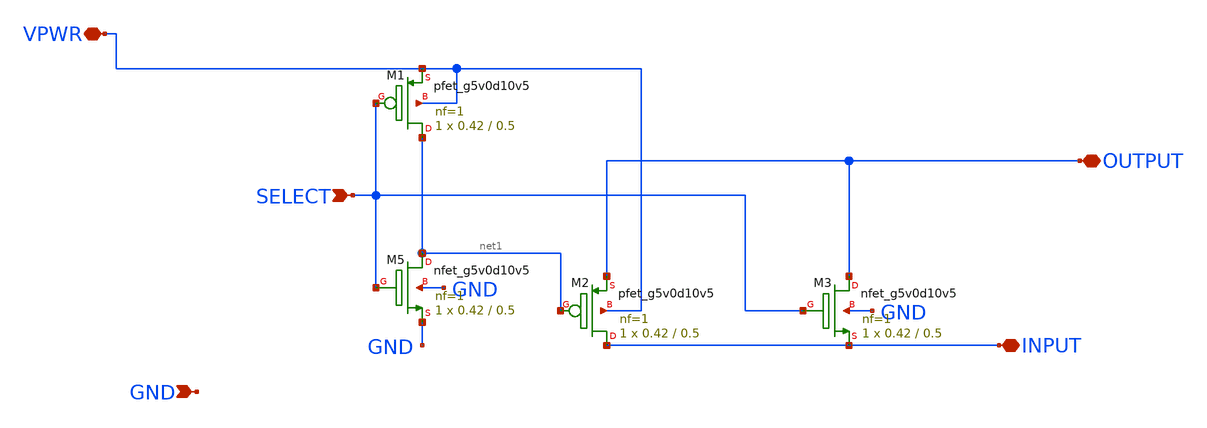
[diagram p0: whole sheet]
** sch_path: sky130_cells/Practice/Capacitor_Array/Schematic/Tgate0.52by0.4.sch
**.subckt Tgate0.52by0.4 VPWR SELECT INPUT OUTPUT GND
*.iopin VPWR
*.ipin SELECT
*.iopin INPUT
*.iopin OUTPUT
*.ipin GND
XM5 net1 SELECT GND GND sky130_fd_pr__nfet_g5v0d10v5 L=0.5 W=0.42 nf=1 ad='int((1 + 1)/2) * 0.42 / 1 * 0.29'
+ as='int((1 + 2)/2) * 0.42 / 1 * 0.29' pd='2*int((1 + 1)/2) * (0.42 / 1 + 0.29)' ps='2*int((1 + 2)/2) * (0.42 / 1 + 0.29)'
+ nrd='0.29 / 0.42 ' nrs='0.29 / 0.42 ' sa=0 sb=0 sd=0 mult=1 m=1
XM1 net1 SELECT VPWR VPWR sky130_fd_pr__pfet_g5v0d10v5 L=0.5 W=0.42 nf=1 ad='int((1 + 1)/2) * 0.42 / 1 * 0.29'
+ as='int((1 + 2)/2) * 0.42 / 1 * 0.29' pd='2*int((1 + 1)/2) * (0.42 / 1 + 0.29)' ps='2*int((1 + 2)/2) * (0.42 / 1 + 0.29)'
+ nrd='0.29 / 0.42 ' nrs='0.29 / 0.42 ' sa=0 sb=0 sd=0 mult=1 m=1
XM2 INPUT net1 OUTPUT VPWR sky130_fd_pr__pfet_g5v0d10v5 L=0.5 W=0.42 nf=1 ad='int((1 + 1)/2) * 0.42 / 1 * 0.29'
+ as='int((1 + 2)/2) * 0.42 / 1 * 0.29' pd='2*int((1 + 1)/2) * (0.42 / 1 + 0.29)' ps='2*int((1 + 2)/2) * (0.42 / 1 + 0.29)'
+ nrd='0.29 / 0.42 ' nrs='0.29 / 0.42 ' sa=0 sb=0 sd=0 mult=1 m=1
XM3 OUTPUT SELECT INPUT GND sky130_fd_pr__nfet_g5v0d10v5 L=0.5 W=0.42 nf=1 ad='int((1 + 1)/2) * 0.42 / 1 * 0.29'
+ as='int((1 + 2)/2) * 0.42 / 1 * 0.29' pd='2*int((1 + 1)/2) * (0.42 / 1 + 0.29)' ps='2*int((1 + 2)/2) * (0.42 / 1 + 0.29)'
+ nrd='0.29 / 0.42 ' nrs='0.29 / 0.42 ' sa=0 sb=0 sd=0 mult=1 m=1
**.ends
.end
